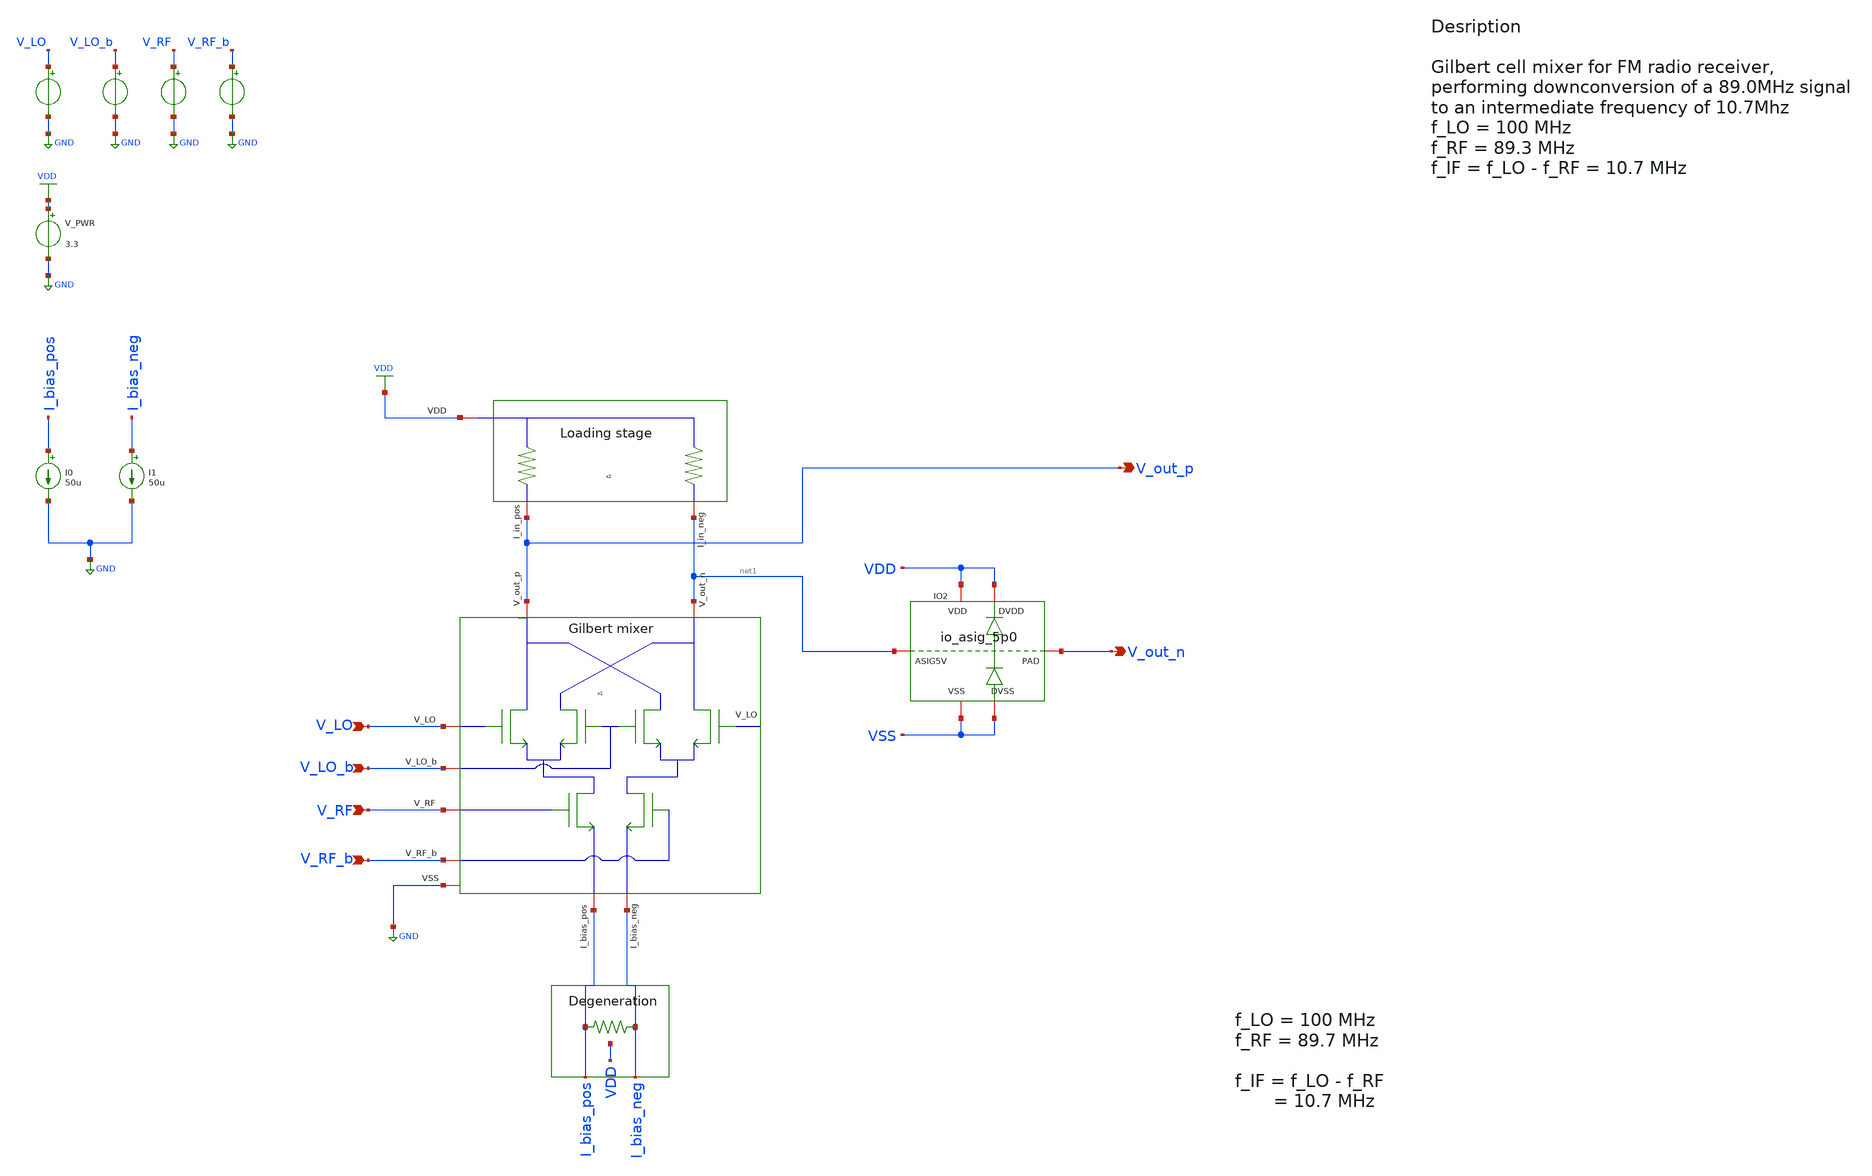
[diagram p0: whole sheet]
** sch_path: src/design_tb/Gilbert_cell_hierarchal_tb.sch
**.subckt Gilbert_cell_hierarchal_tb V_LO V_LO_b V_RF V_RF_b V_out_p V_out_n
*.ipin V_LO
*.ipin V_LO_b
*.ipin V_RF
*.ipin V_RF_b
*.opin V_out_p
*.opin V_out_n
V_PWR VDD GND 3.3
.save i(v_pwr)
V_LO V_LO GND pulse(0 1.5 0 1p 1p 0.25n 0.5n)
.save i(v_lo)
V_LO_b V_LO_b GND pulse(0 1.5 0 1p 1p 0.25n 0.5n)
.save i(v_lo_b)
V_RF V_RF GND sin( 1 1 1 0 )
.save i(v_rf)
V_RF_b V_RF_b GND sin( 1 1 1 0 0 180 )
.save i(v_rf_b)
I0 I_bias_pos GND 50u
I1 I_bias_neg GND 50u
x1 net1 V_out_p V_LO V_LO_b V_RF V_RF_b I_bias_pos I_bias_neg GND
+ Gilbert_cell_hierarchal_mixing_stage
x2 V_out_p net1 VDD Gilbert_cell_hierarchal_loading_stage
XR_load_3 I_bias_pos I_bias_neg VDD pplus_u r_width=0.5e-6 r_length=5e-6 m=1
XIO2 VSS VDD VSS VDD V_out_n net1 gf180mcu_fd_io__asig_5p0_extracted
**** begin user architecture code

.include $::PROJECT_ROOT/src/Chipathon2025_pads/xschem/gf180mcu_fd_io.spice
.include $::PROJECT_ROOT/src/Chipathon2025_pads/xschem/gf180mcu_fd_io__asig_5p0_extracted.spice
.include $::180MCU_MODELS/design.ngspice
.lib $::180MCU_MODELS/sm141064.ngspice typical
.lib $::180MCU_MODELS/sm141064.ngspice mimcap_typical
.lib $::180MCU_MODELS/sm141064.ngspice cap_mim
.lib $::180MCU_MODELS/sm141064.ngspice res_typical
.lib $::180MCU_MODELS/sm141064.ngspice diode_typical
.lib $::180MCU_MODELS/sm141064.ngspice bjt_typical
.lib $::180MCU_MODELS/sm141064.ngspice moscap_typical
.lib $::180MCU_MODELS/sm141064.ngspice mimcap_typical



* let sets vectors to a plot, while set sets a variable, globally accessible in .control
.control

    * Set frequency and amplitude variables to proper values from within the control sequence
    * sine-wave LO
    * set cm_lo = 0.5
    * set freq_lo = 2.50G
    * set amp_lo = 0.5
    * alter @V_LO[sin] = [ $cm_lo $amp_lo $freq_lo 0 ]
    * alter @V_LO_b[sin] = [ $cm_lo $amp_lo $freq_lo 0 0 180 ]

    set freq_lo = 100Meg
    set cm_lo = 1.8
    set amp_lo = 0.4

    set cm_rf  = 1.2
    set freq_rf = 89.3Meg
    * set freq_rf = 10.7Meg
    set amp_rf  = 0.1

    * set the parameters to the voltage sources
    alter @V_LO[sin] = [ $cm_lo $amp_lo $freq_lo 0 ]
    alter @V_LO_b[sin] = [ $cm_lo $amp_lo $freq_lo 0 0 180 ]
    alter @V_RF[sin] = [ $cm_rf $amp_rf $freq_rf 0 ]
    alter @V_RF_b[sin] = [ $cm_rf $amp_rf $freq_rf 0 0 180 ]

    save all

    * operating point
    op
    * show

    write Gilbert_cell_hierarchal_sim.raw

    set appendwrite

    * Transient analysis to observe mixing operation
    tran 3p 0.5u
    write Gilbert_cell_hierarchal_sim.raw

    * Calculate differential output for conversion gain measurement
    let v_out_diff = v(v_out_p)-v(v_out_n)
    let v_rf_diff = v(v_rf)-v(v_rf_b)
    let v_lo_diff = v(v_lo)-v(v_lo_b)


    * Extract IF component at 100MHz using FFT
    linearize v_out_diff v_rf_diff v_lo_diff
    let time_step = 1e-12
    let sample_freq = 1/time_step
    let npts = length(v_out_diff)
    let freq_res = sample_freq/npts


    fft v_out_diff v_rf_diff v_lo_diff

    * print everything, sanity check
    * set     ; print all available global (?) variables (?)
    * setplot ; print all plots
    * display ; print variables available in current plot

    let freq_res = tran2.freq_res
    let freq_if = abs ( $freq_lo - $freq_rf )

    * Define bandwidth for power integration (10MHz around nominal frequencies).
    *  To improve resolution increase time of tran simulation, reduce time step, in order to reduce
+ FFT resolution
    let bandwidth = 15e6
    let bin_width = floor(bandwidth/freq_res + 0.5)
    print bin_width


    * Find center bins for RF and IF frequencies
    let rf_center_bin = floor( $freq_rf/freq_res + 0.5 )
    let if_center_bin = floor( freq_if/freq_res + 0.5 )
    print freq_if
    print freq_res
    print abs(v_out_diff[if_center_bin])
    print abs(v_out_diff[if_center_bin-1])
    print abs(v_out_diff[if_center_bin+1])



    * Calculate power by summing magnitude squared over the bandwidth
    * RF power integration (±10MHz around freq_rf)
    let rf_power_total = 0
    let i = rf_center_bin - bin_width
    while i <= rf_center_bin + bin_width
        if i>0 & i < length(v_rf_diff)
            let bin_freq = i * freq_res
            * print bin_freq
            * print abs(v_rf_diff[i])
            let rf_power_total = rf_power_total + abs(v_rf_diff[i])^2
        end
        let i = i + 1
    end

    * IF power integration (±10MHz around freq_if)
    let if_power_total = 0
    let j = if_center_bin - bin_width
    while j <= if_center_bin + bin_width
        if j >= 0 & j < length(v_out_diff)
            let bin_freq = j * freq_res
            print bin_freq
            print abs(v_out_diff[j])
            let if_power_total = if_power_total + abs(v_out_diff[j])^2
        end
        let j = j + 1
    end

    print if_power_total
    print rf_power_total

    let conversion_gain_db = 10*log10(if_power_total/rf_power_total)
    print conversion_gain_db

    write Gilbert_cell_hierarchal_sim.raw

.endc


**** end user architecture code
**.ends

* expanding   symbol:
*+  /home/vasil/Downloads/SSCS_PICO_2025/src/design_xsch/Gilbert_cell_hierarchal_loading_stage.sym # of pins=3
** sym_path: src/design_xsch/Gilbert_cell_hierarchal_loading_stage.sym
** sch_path: src/design_xsch/Gilbert_cell_hierarchal_loading_stage.sch
.subckt Gilbert_cell_hierarchal_loading_stage I_in_pos I_in_neg VDD
*.iopin I_in_neg
*.iopin I_in_pos
*.iopin VDD
XR_load_2 I_in_pos VDD VDD ppolyf_u_1k r_width=0.5e-6 r_length=10e-6 m=1
XR_load_1 I_in_neg VDD VDD ppolyf_u_1k r_width=0.5e-6 r_length=10e-6 m=1
.ends

.GLOBAL VDD
.GLOBAL GND
.end
